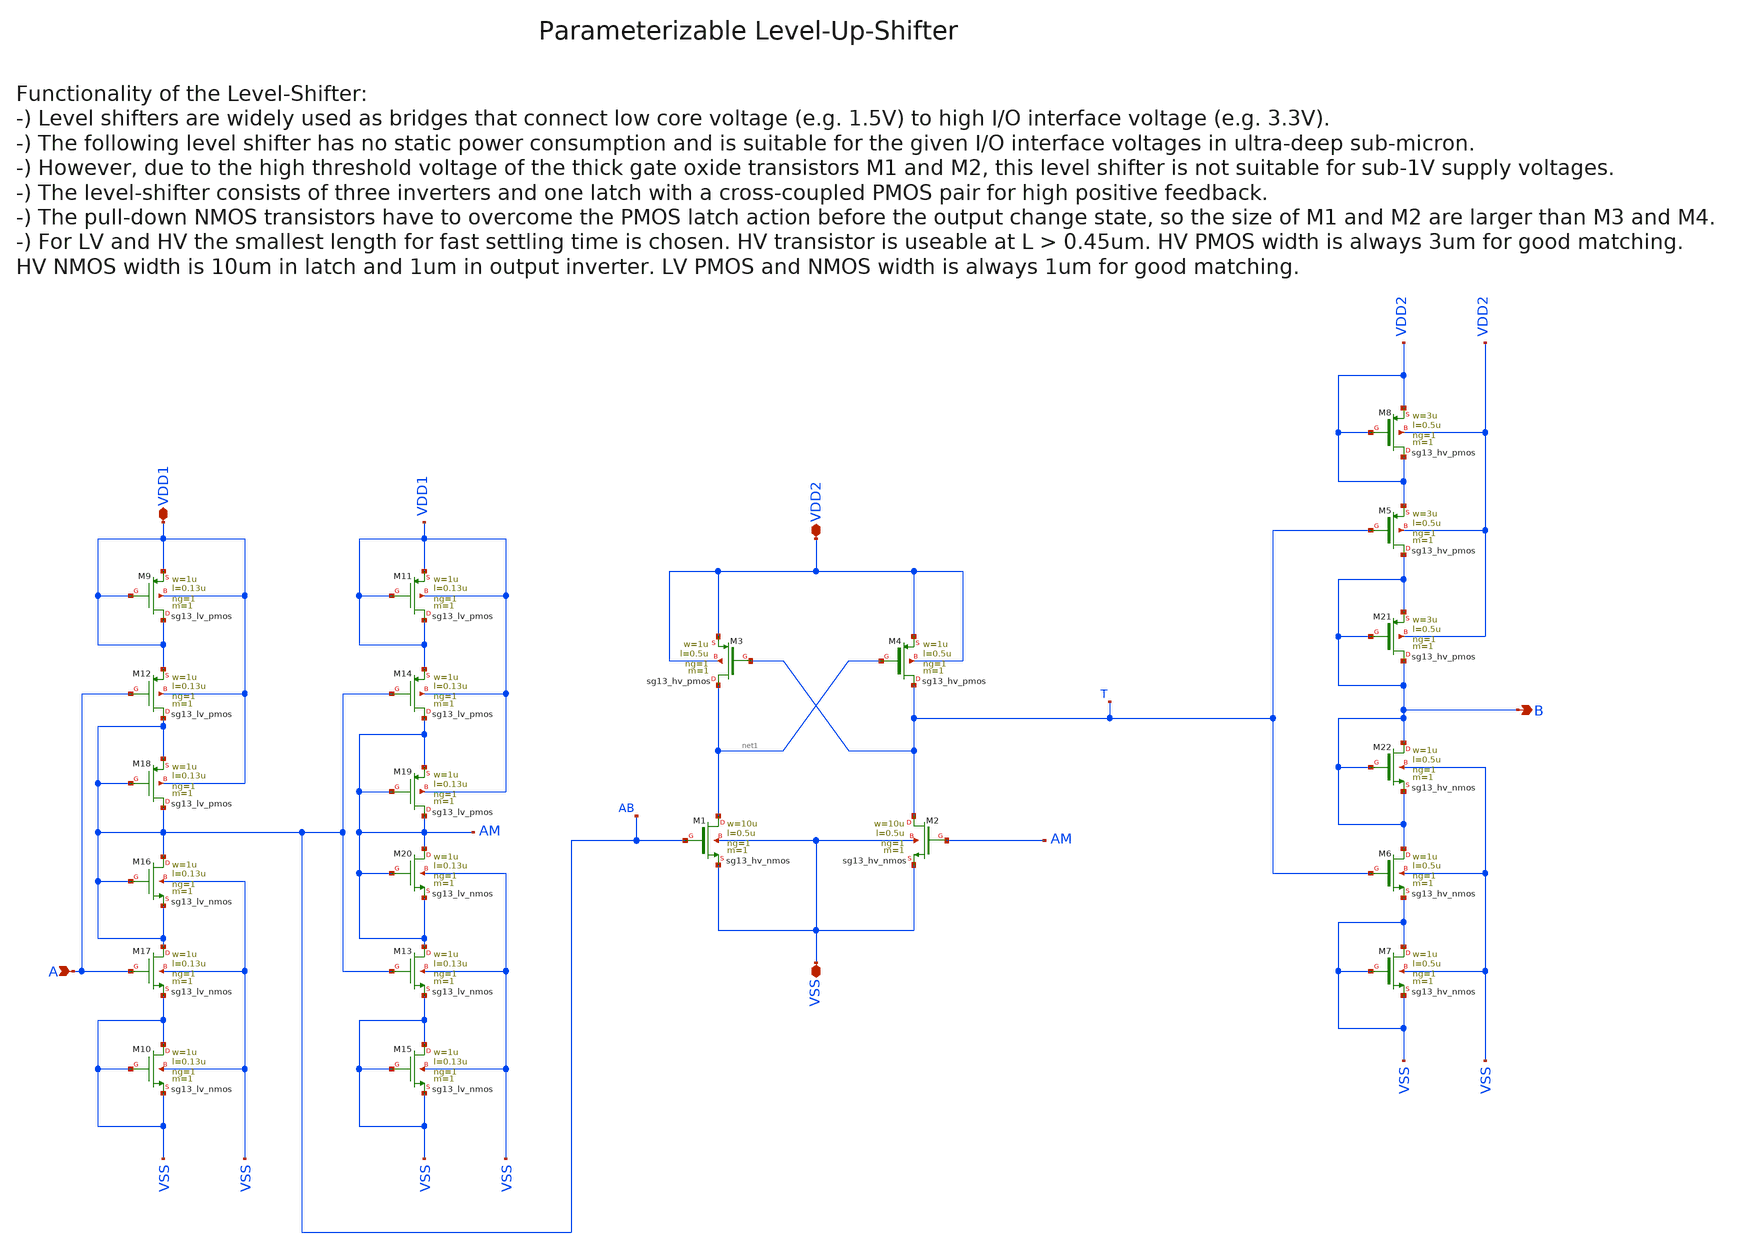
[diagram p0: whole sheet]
** sch_path: macros/heichips26_ook/macros/ook_analog_system/schematic/xschem/level_up_shifter.sch
**.subckt level_up_shifter VSS VDD2 B A VDD1
*.iopin VSS
*.iopin VDD2
*.opin B
*.ipin A
*.iopin VDD1
XM1 net1 AB VSS VSS sg13_hv_nmos w=10u l=0.5u ng=1 m=1 mm_ok=1
XM4 T net1 VDD2 VDD2 sg13_hv_pmos w=1u l=0.5u ng=1 m=1 mm_ok=1
XM3 net1 T VDD2 VDD2 sg13_hv_pmos w=1u l=0.5u ng=1 m=1 mm_ok=1
XM2 T AM VSS VSS sg13_hv_nmos w=10u l=0.5u ng=1 m=1 mm_ok=1
XM5 B T VDD2 VDD2 sg13_hv_pmos w=3u l=0.5u ng=1 m=1 mm_ok=1
XM6 B T VSS VSS sg13_hv_nmos w=1u l=0.5u ng=1 m=1 mm_ok=1
XM7 VSS VSS VSS VSS sg13_hv_nmos w=1u l=0.5u ng=1 m=1 mm_ok=1
XM8 VDD2 VDD2 VDD2 VDD2 sg13_hv_pmos w=3u l=0.5u ng=1 m=1 mm_ok=1
XM9 VDD1 VDD1 VDD1 VDD1 sg13_lv_pmos w=1u l=0.13u ng=1 m=1 mm_ok=1
XM12 AB A VDD1 VDD1 sg13_lv_pmos w=1u l=0.13u ng=1 m=1 mm_ok=1
XM10 VSS VSS VSS VSS sg13_lv_nmos w=1u l=0.13u ng=1 m=1 mm_ok=1
XM11 VDD1 VDD1 VDD1 VDD1 sg13_lv_pmos w=1u l=0.13u ng=1 m=1 mm_ok=1
XM14 AM AB VDD1 VDD1 sg13_lv_pmos w=1u l=0.13u ng=1 m=1 mm_ok=1
XM15 VSS VSS VSS VSS sg13_lv_nmos w=1u l=0.13u ng=1 m=1 mm_ok=1
XM17 AB A VSS VSS sg13_lv_nmos w=1u l=0.13u ng=1 m=1 mm_ok=1
XM13 AM AB VSS VSS sg13_lv_nmos w=1u l=0.13u ng=1 m=1 mm_ok=1
XM16 AB AB AB VSS sg13_lv_nmos w=1u l=0.13u ng=1 m=1 mm_ok=1
XM18 AB AB AB VDD1 sg13_lv_pmos w=1u l=0.13u ng=1 m=1 mm_ok=1
XM19 AM AM AM VDD1 sg13_lv_pmos w=1u l=0.13u ng=1 m=1 mm_ok=1
XM20 AM AM AM VSS sg13_lv_nmos w=1u l=0.13u ng=1 m=1 mm_ok=1
XM21 B B B VDD2 sg13_hv_pmos w=3u l=0.5u ng=1 m=1 mm_ok=1
XM22 B B B VSS sg13_hv_nmos w=1u l=0.5u ng=1 m=1 mm_ok=1
**.ends
.end
